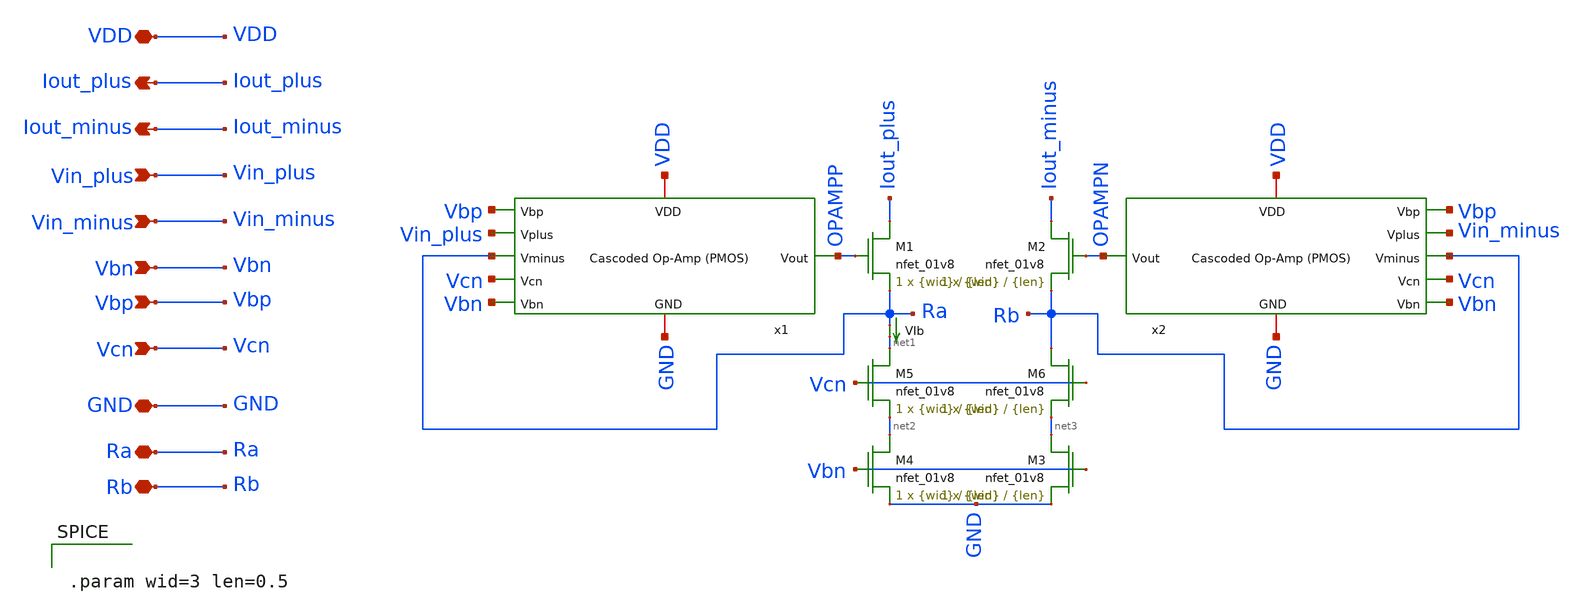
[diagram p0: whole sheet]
** sch_path: final/schematics/VI_input.sch
**.subckt VI_input Iout_plus Iout_minus VDD Vin_plus Vin_minus Vbn GND Ra Rb Vbp Vcn
*.opin Iout_plus
*.opin Iout_minus
*.iopin VDD
*.ipin Vin_plus
*.ipin Vin_minus
*.ipin Vbn
*.iopin GND
*.iopin Ra
*.iopin Rb
*.ipin Vbp
*.ipin Vcn
XM1 Iout_plus OPAMPP Ra GND sky130_fd_pr__nfet_01v8 L={len} W={wid} nf=1 ad='int((nf+1)/2) * W/nf * 0.29'
+ as='int((nf+2)/2) * W/nf * 0.29' pd='2*int((nf+1)/2) * (W/nf + 0.29)' ps='2*int((nf+2)/2) * (W/nf + 0.29)'
+ nrd='0.29 / W' nrs='0.29 / W' sa=0 sb=0 sd=0 mult=1 m=1
XM2 Iout_minus OPAMPN Rb GND sky130_fd_pr__nfet_01v8 L={len} W={wid} nf=1 ad='int((nf+1)/2) * W/nf * 0.29'
+ as='int((nf+2)/2) * W/nf * 0.29' pd='2*int((nf+1)/2) * (W/nf + 0.29)' ps='2*int((nf+2)/2) * (W/nf + 0.29)'
+ nrd='0.29 / W' nrs='0.29 / W' sa=0 sb=0 sd=0 mult=1 m=1
x1 Vbp Vin_plus Ra Vcn Vbn VDD GND OPAMPP cascoded_opamp_pmos
x2 Vbp Vin_minus Rb Vcn Vbn VDD GND OPAMPN cascoded_opamp_pmos
XM3 net3 Vbn GND GND sky130_fd_pr__nfet_01v8 L={len} W={wid} nf=1 ad='int((nf+1)/2) * W/nf * 0.29' as='int((nf+2)/2) * W/nf * 0.29'
+ pd='2*int((nf+1)/2) * (W/nf + 0.29)' ps='2*int((nf+2)/2) * (W/nf + 0.29)' nrd='0.29 / W' nrs='0.29 / W'
+ sa=0 sb=0 sd=0 mult=1 m=1
XM4 net2 Vbn GND GND sky130_fd_pr__nfet_01v8 L={len} W={wid} nf=1 ad='int((nf+1)/2) * W/nf * 0.29' as='int((nf+2)/2) * W/nf * 0.29'
+ pd='2*int((nf+1)/2) * (W/nf + 0.29)' ps='2*int((nf+2)/2) * (W/nf + 0.29)' nrd='0.29 / W' nrs='0.29 / W'
+ sa=0 sb=0 sd=0 mult=1 m=1
VIb Ra net1 0
.save i(vib)
XM5 net1 Vcn net2 GND sky130_fd_pr__nfet_01v8 L={len} W={wid} nf=1 ad='int((nf+1)/2) * W/nf * 0.29' as='int((nf+2)/2) * W/nf * 0.29'
+ pd='2*int((nf+1)/2) * (W/nf + 0.29)' ps='2*int((nf+2)/2) * (W/nf + 0.29)' nrd='0.29 / W' nrs='0.29 / W'
+ sa=0 sb=0 sd=0 mult=1 m=1
XM6 Rb Vcn net3 GND sky130_fd_pr__nfet_01v8 L={len} W={wid} nf=1 ad='int((nf+1)/2) * W/nf * 0.29' as='int((nf+2)/2) * W/nf * 0.29'
+ pd='2*int((nf+1)/2) * (W/nf + 0.29)' ps='2*int((nf+2)/2) * (W/nf + 0.29)' nrd='0.29 / W' nrs='0.29 / W'
+ sa=0 sb=0 sd=0 mult=1 m=1
**** begin user architecture code


.param wid=3 len=0.5


**** end user architecture code
**.ends
.end
